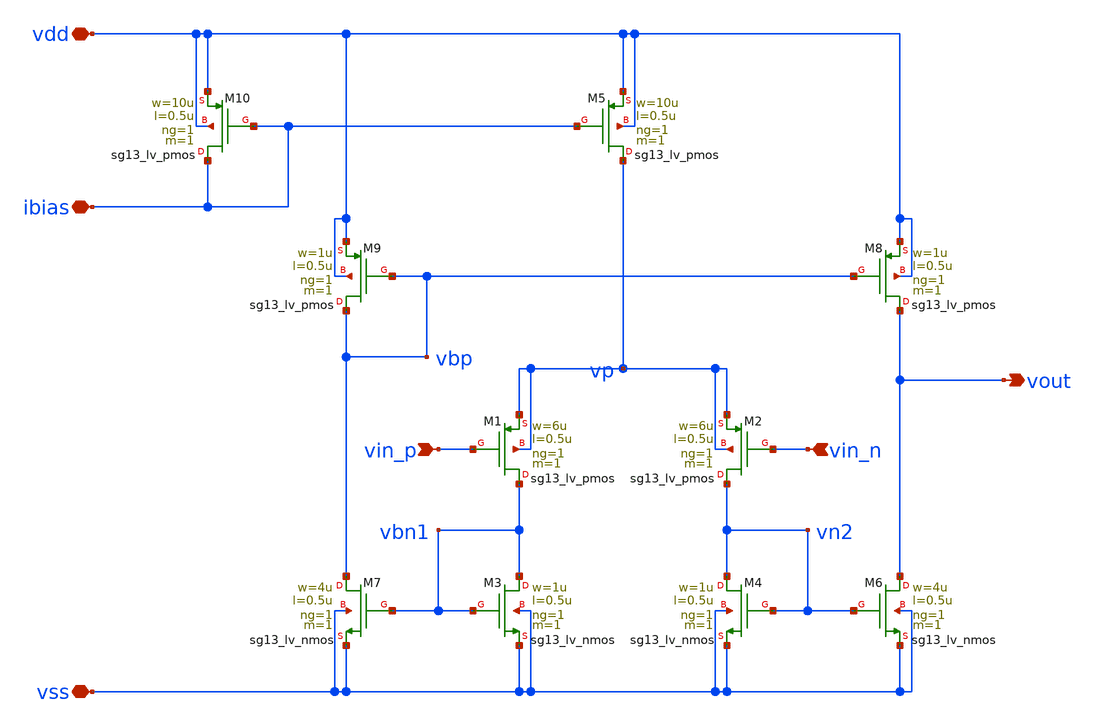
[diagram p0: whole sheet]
** sch_path: SSDOR_1.2V_v2/components/cgenerator/ota_comparator.sch
**.subckt ota_comparator vdd vss ibias vin_p vin_n vout
*.iopin vdd
*.iopin vss
*.iopin ibias
*.ipin vin_p
*.ipin vin_n
*.opin vout
XM1 vbn1 vin_p vp vp sg13_lv_pmos w=6u l=0.5u ng=1 m=1 mm_ok=1
XM2 vn2 vin_n vp vp sg13_lv_pmos w=6u l=0.5u ng=1 m=1 mm_ok=1
XM5 vp ibias vdd vdd sg13_lv_pmos w=10u l=0.5u ng=1 m=1 mm_ok=1
XM3 vbn1 vbn1 vss vss sg13_lv_nmos w=1u l=0.5u ng=1 m=1 mm_ok=1
XM4 vn2 vn2 vss vss sg13_lv_nmos w=1u l=0.5u ng=1 m=1 mm_ok=1
XM6 vout vn2 vss vss sg13_lv_nmos w=4u l=0.5u ng=1 m=1 mm_ok=1
XM7 vbp vbn1 vss vss sg13_lv_nmos w=4u l=0.5u ng=1 m=1 mm_ok=1
XM8 vout vbp vdd vdd sg13_lv_pmos w=1u l=0.5u ng=1 m=1 mm_ok=1
XM9 vbp vbp vdd vdd sg13_lv_pmos w=1u l=0.5u ng=1 m=1 mm_ok=1
XM10 ibias ibias vdd vdd sg13_lv_pmos w=10u l=0.5u ng=1 m=1 mm_ok=1
**.ends
.end
